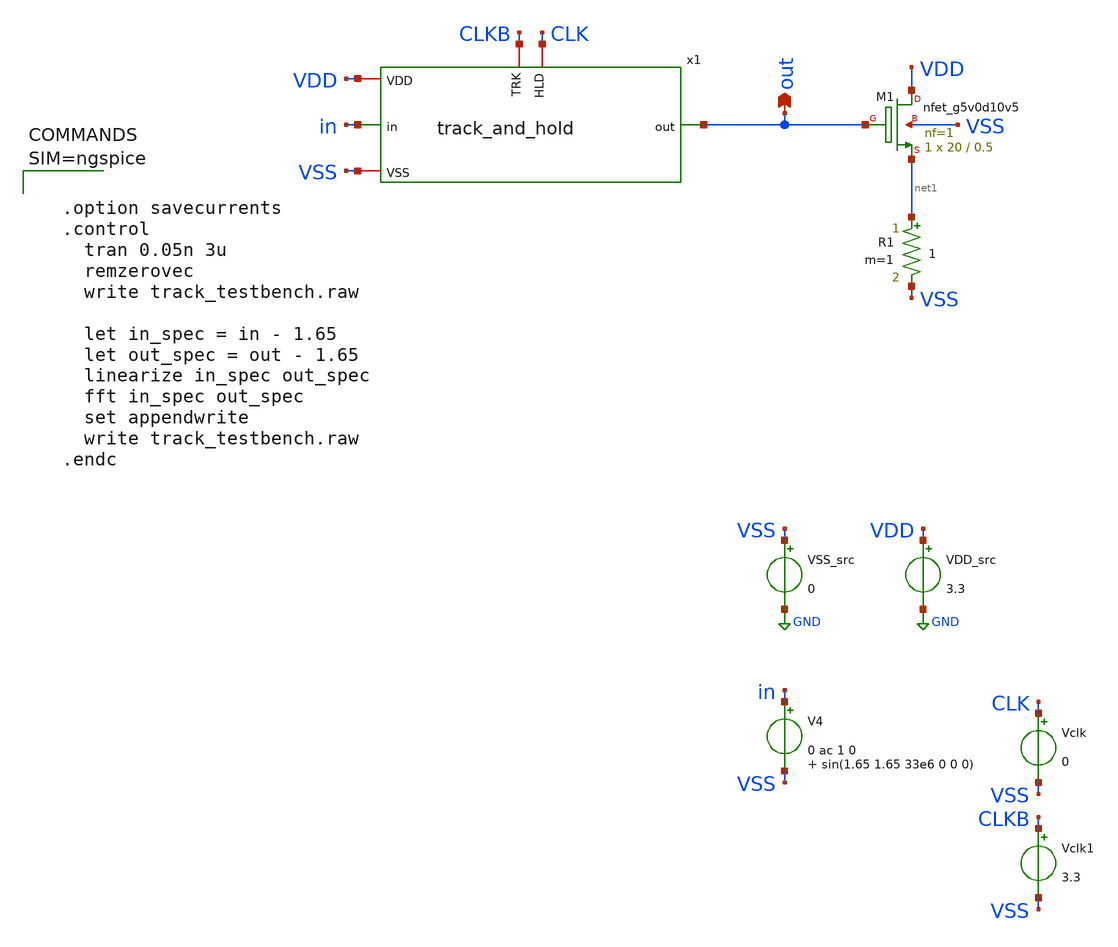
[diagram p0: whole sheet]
** sch_path: xschem/track_testbench.sch
**.subckt track_testbench out
*.opin out
VDD_src VDD GND 3.3
VSS_src VSS GND 0
V4 in VSS 0 ac 1 0 sin(1.65 1.65 33e6 0 0 0)
XM1 VDD out net1 VSS sky130_fd_pr__nfet_g5v0d10v5 L=0.5 W=20 nf=1 ad='int((nf+1)/2) * W/nf * 0.29' as='int((nf+2)/2) * W/nf * 0.29'
+ pd='2*int((nf+1)/2) * (W/nf + 0.29)' ps='2*int((nf+2)/2) * (W/nf + 0.29)' nrd='0.29 / W' nrs='0.29 / W'
+ sa=0 sb=0 sd=0 mult=1 m=1
R1 net1 VSS 1 m=1
Vclk CLK VSS 0
Vclk1 CLKB VSS 3.3
x1 CLK CLKB VDD VSS out in track_and_hold
**** begin user architecture code

** opencircuitdesign pdks install
.lib $::SKYWATER_MODELS/sky130.lib.spice tt





  .option savecurrents
  .control
    tran 0.05n 3u
    remzerovec
    write track_testbench.raw

    let in_spec = in - 1.65
    let out_spec = out - 1.65
    linearize in_spec out_spec
    fft in_spec out_spec
    set appendwrite
    write track_testbench.raw
  .endc



**** end user architecture code
**.ends

* expanding   symbol:  track_and_hold.sym # of pins=6
** sym_path: xschem/track_and_hold.sym
** sch_path: xschem/track_and_hold.sch
.subckt track_and_hold HLD TRK VDD VSS out in
*.iopin VSS
*.iopin VDD
*.ipin in
*.opin out
*.iopin TRK
*.iopin HLD
XC1 out VSS sky130_fd_pr__cap_mim_m3_1 W=5 L=5 MF=1 m=1
V1 net2 net5 3.3
XM1 out net1 in VSS sky130_fd_pr__nfet_g5v0d10v5 L=0.5 W=1 nf=1 ad='int((nf+1)/2) * W/nf * 0.29' as='int((nf+2)/2) * W/nf * 0.29'
+ pd='2*int((nf+1)/2) * (W/nf + 0.29)' ps='2*int((nf+2)/2) * (W/nf + 0.29)' nrd='0.29 / W' nrs='0.29 / W'
+ sa=0 sb=0 sd=0 mult=1 m=1
R1 VDD VSS 1G m=1
**** begin user architecture code



.model switch1 sw vt=1.65 vh=0 ron=1 roff=1G



**** end user architecture code
V2 net6 net3 3.3
XM1p out net4 in VDD sky130_fd_pr__pfet_g5v0d10v5 L=0.5 W=1.28 nf=1 ad='int((nf+1)/2) * W/nf * 0.29'
+ as='int((nf+2)/2) * W/nf * 0.29' pd='2*int((nf+1)/2) * (W/nf + 0.29)' ps='2*int((nf+2)/2) * (W/nf + 0.29)'
+ nrd='0.29 / W' nrs='0.29 / W' sa=0 sb=0 sd=0 mult=1 m=1
XM4 VSS HLD net1 VSS sky130_fd_pr__nfet_g5v0d10v5 L=0.5 W=1 nf=1 ad='int((nf+1)/2) * W/nf * 0.29' as='int((nf+2)/2) * W/nf * 0.29'
+ pd='2*int((nf+1)/2) * (W/nf + 0.29)' ps='2*int((nf+2)/2) * (W/nf + 0.29)' nrd='0.29 / W' nrs='0.29 / W'
+ sa=0 sb=0 sd=0 mult=1 m=1
XM4p net4 TRK VDD VDD sky130_fd_pr__pfet_g5v0d10v5 L=0.5 W=2 nf=1 ad='int((nf+1)/2) * W/nf * 0.29' as='int((nf+2)/2) * W/nf * 0.29'
+ pd='2*int((nf+1)/2) * (W/nf + 0.29)' ps='2*int((nf+2)/2) * (W/nf + 0.29)' nrd='0.29 / W' nrs='0.29 / W'
+ sa=0 sb=0 sd=0 mult=1 m=1
XM2 net1 HLD net2 net2 sky130_fd_pr__pfet_g5v0d10v5 L=0.5 W=2 nf=1 ad='int((nf+1)/2) * W/nf * 0.29' as='int((nf+2)/2) * W/nf * 0.29'
+ pd='2*int((nf+1)/2) * (W/nf + 0.29)' ps='2*int((nf+2)/2) * (W/nf + 0.29)' nrd='0.29 / W' nrs='0.29 / W'
+ sa=0 sb=0 sd=0 mult=1 m=1
XM2p net3 TRK net4 net3 sky130_fd_pr__nfet_g5v0d10v5 L=0.5 W=1 nf=1 ad='int((nf+1)/2) * W/nf * 0.29'
+ as='int((nf+2)/2) * W/nf * 0.29' pd='2*int((nf+1)/2) * (W/nf + 0.29)' ps='2*int((nf+2)/2) * (W/nf + 0.29)'
+ nrd='0.29 / W' nrs='0.29 / W' sa=0 sb=0 sd=0 mult=1 m=1
XM3 in net1 net5 VSS sky130_fd_pr__nfet_g5v0d10v5 L=0.5 W=1 nf=1 ad='int((nf+1)/2) * W/nf * 0.29' as='int((nf+2)/2) * W/nf * 0.29'
+ pd='2*int((nf+1)/2) * (W/nf + 0.29)' ps='2*int((nf+2)/2) * (W/nf + 0.29)' nrd='0.29 / W' nrs='0.29 / W'
+ sa=0 sb=0 sd=0 mult=1 m=1
XM6 net5 HLD VSS VSS sky130_fd_pr__nfet_g5v0d10v5 L=0.5 W=1 nf=1 ad='int((nf+1)/2) * W/nf * 0.29' as='int((nf+2)/2) * W/nf * 0.29'
+ pd='2*int((nf+1)/2) * (W/nf + 0.29)' ps='2*int((nf+2)/2) * (W/nf + 0.29)' nrd='0.29 / W' nrs='0.29 / W'
+ sa=0 sb=0 sd=0 mult=1 m=1
XM3p net6 net4 in VDD sky130_fd_pr__pfet_g5v0d10v5 L=0.5 W=2 nf=1 ad='int((nf+1)/2) * W/nf * 0.29' as='int((nf+2)/2) * W/nf * 0.29'
+ pd='2*int((nf+1)/2) * (W/nf + 0.29)' ps='2*int((nf+2)/2) * (W/nf + 0.29)' nrd='0.29 / W' nrs='0.29 / W'
+ sa=0 sb=0 sd=0 mult=1 m=1
XM6p VDD TRK net6 VDD sky130_fd_pr__pfet_g5v0d10v5 L=0.5 W=2 nf=1 ad='int((nf+1)/2) * W/nf * 0.29' as='int((nf+2)/2) * W/nf * 0.29'
+ pd='2*int((nf+1)/2) * (W/nf + 0.29)' ps='2*int((nf+2)/2) * (W/nf + 0.29)' nrd='0.29 / W' nrs='0.29 / W'
+ sa=0 sb=0 sd=0 mult=1 m=1
.ends

.GLOBAL GND
.end
